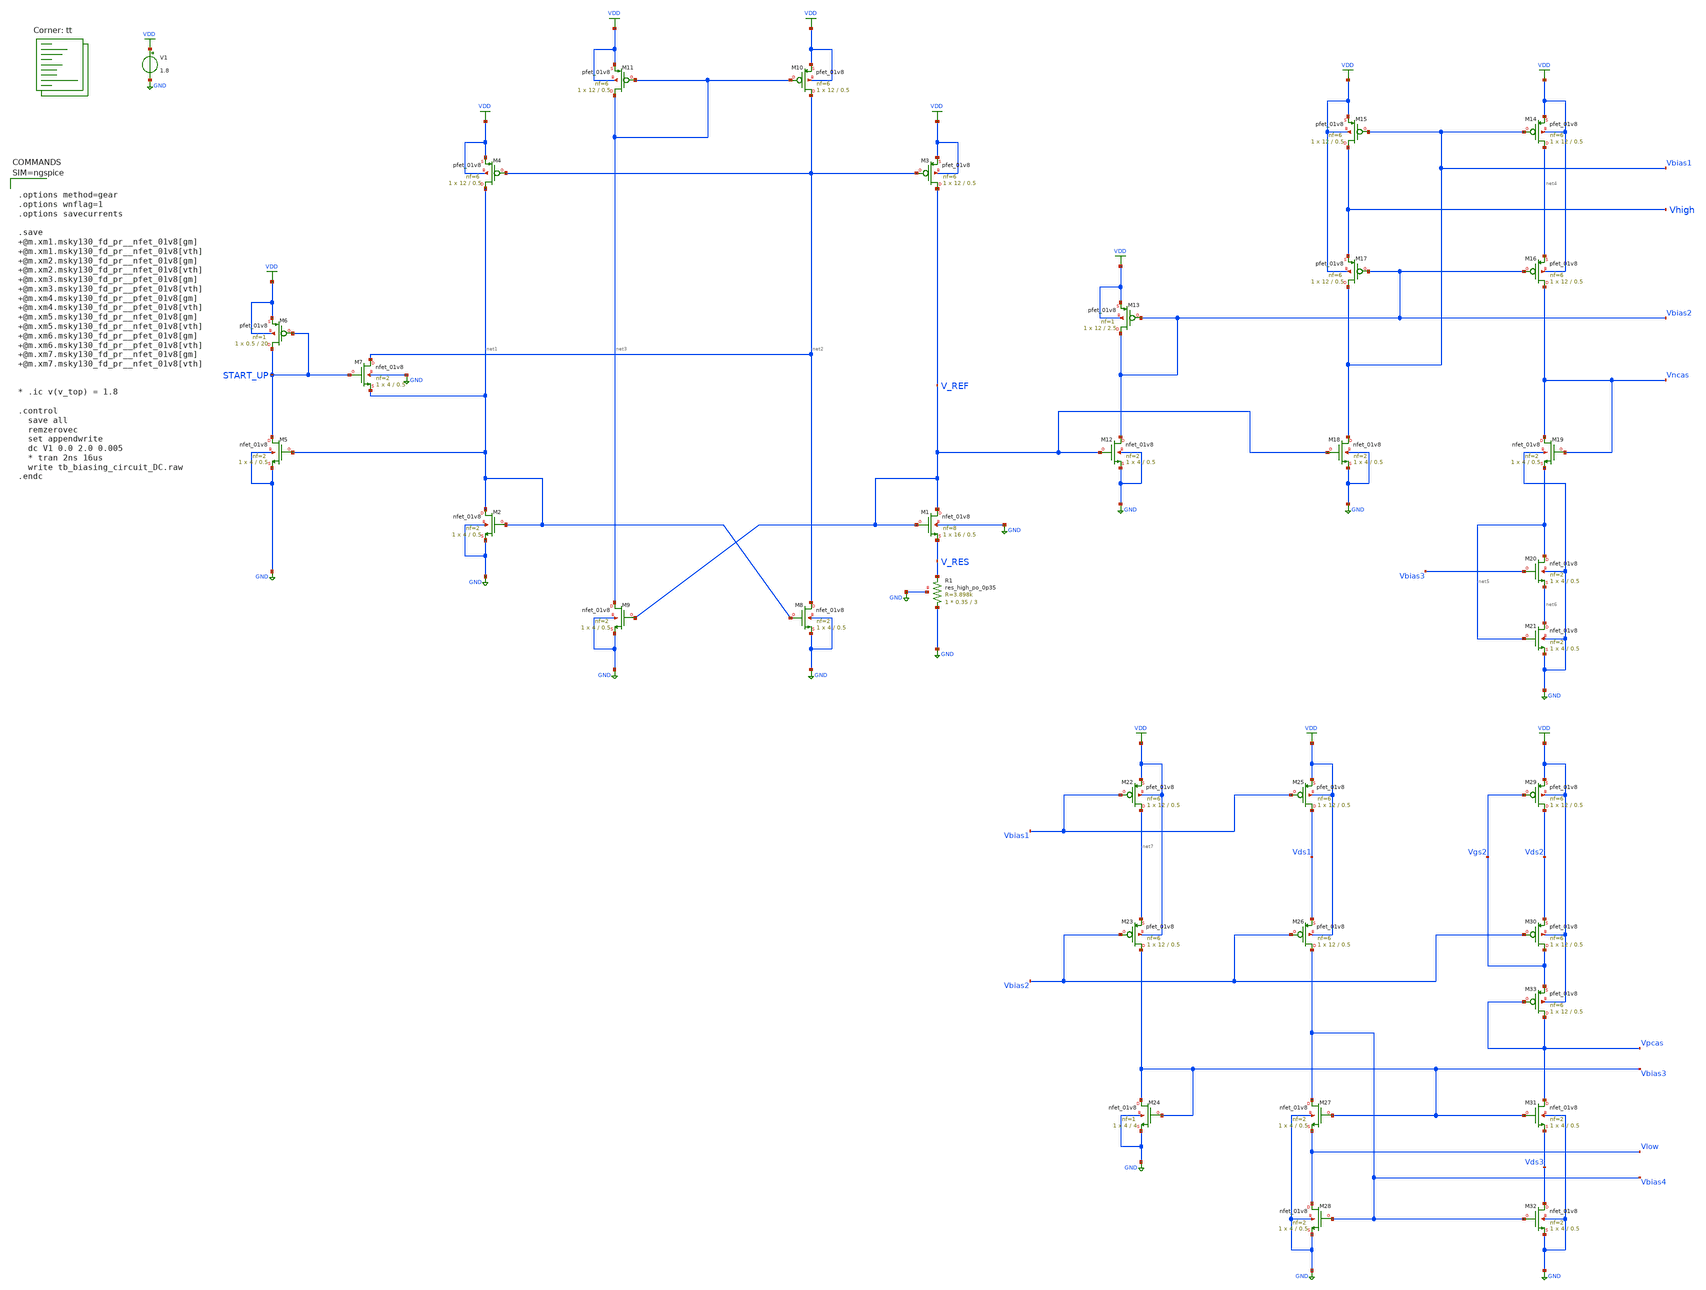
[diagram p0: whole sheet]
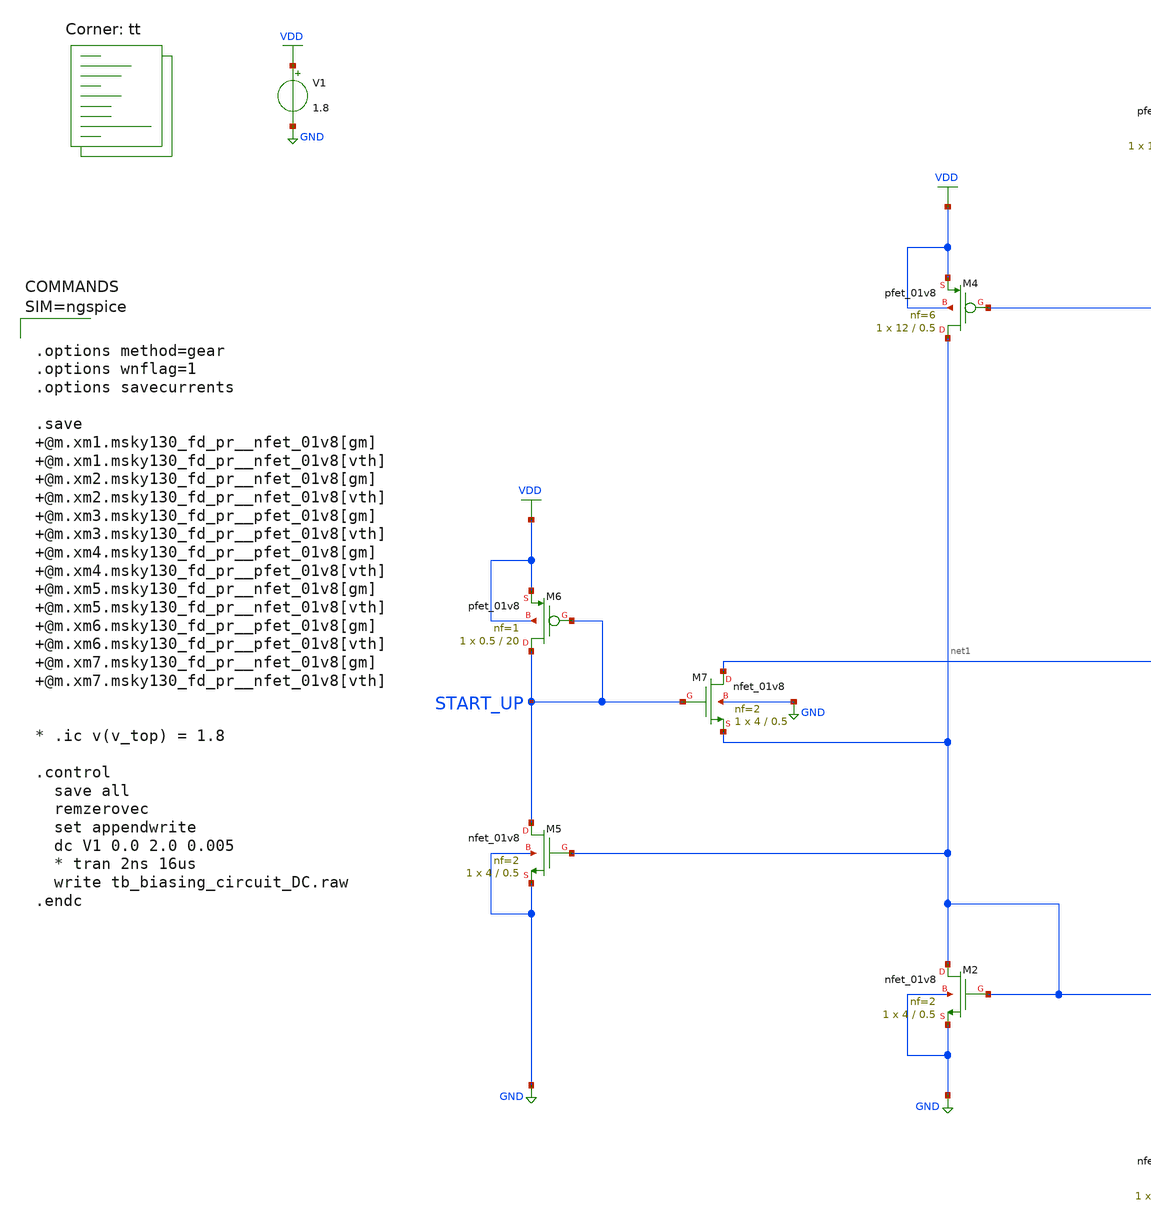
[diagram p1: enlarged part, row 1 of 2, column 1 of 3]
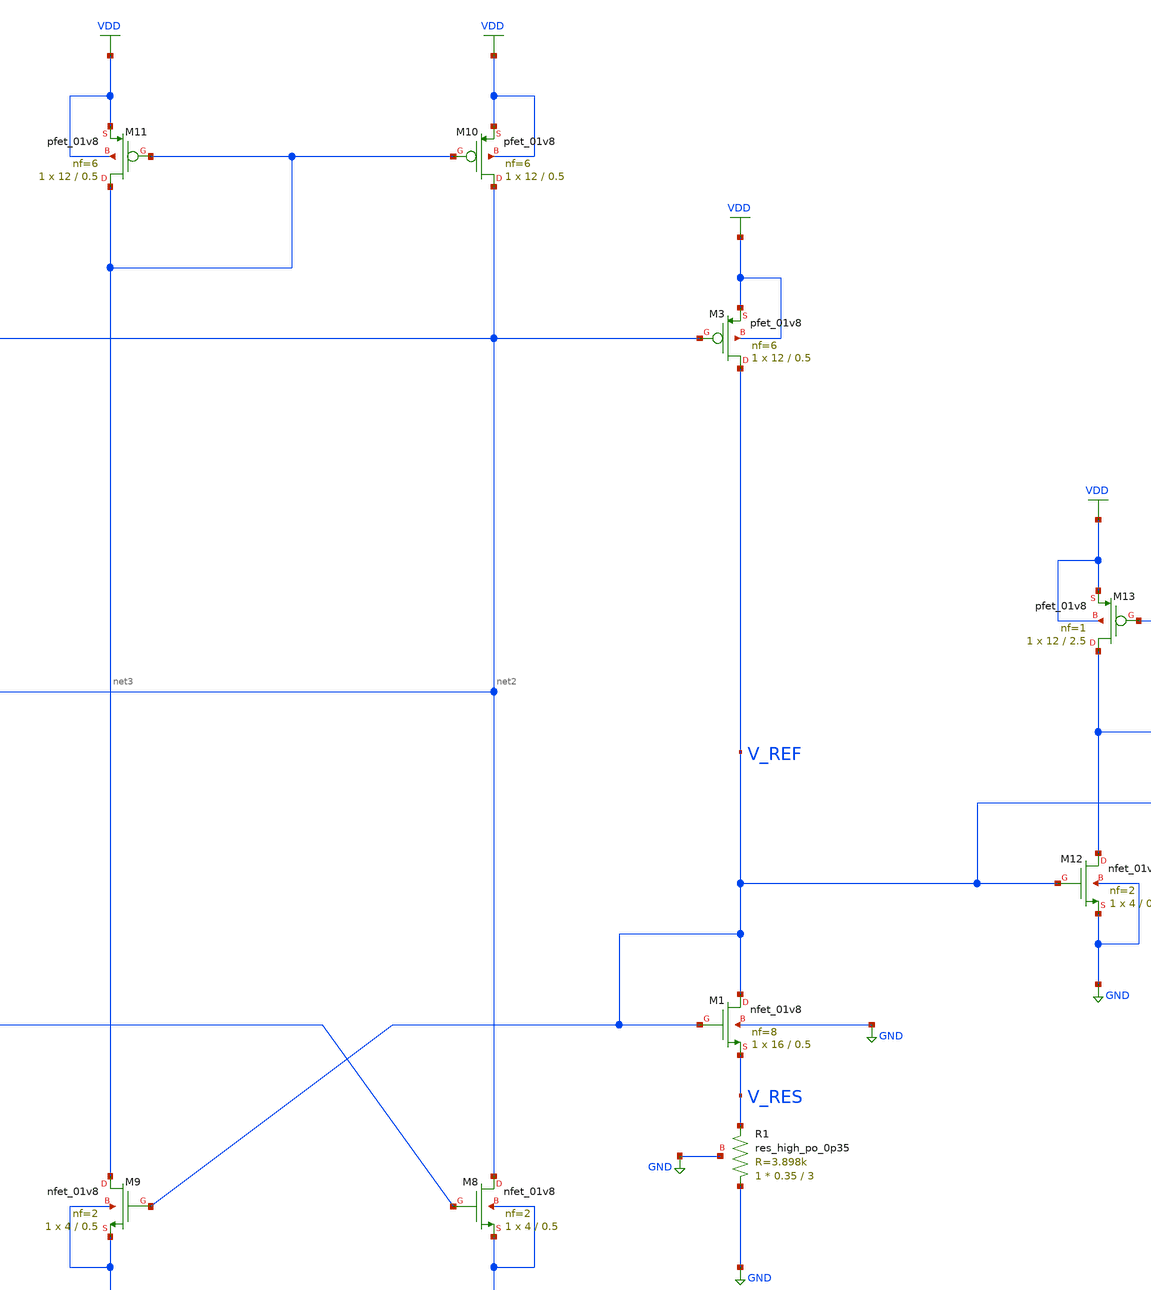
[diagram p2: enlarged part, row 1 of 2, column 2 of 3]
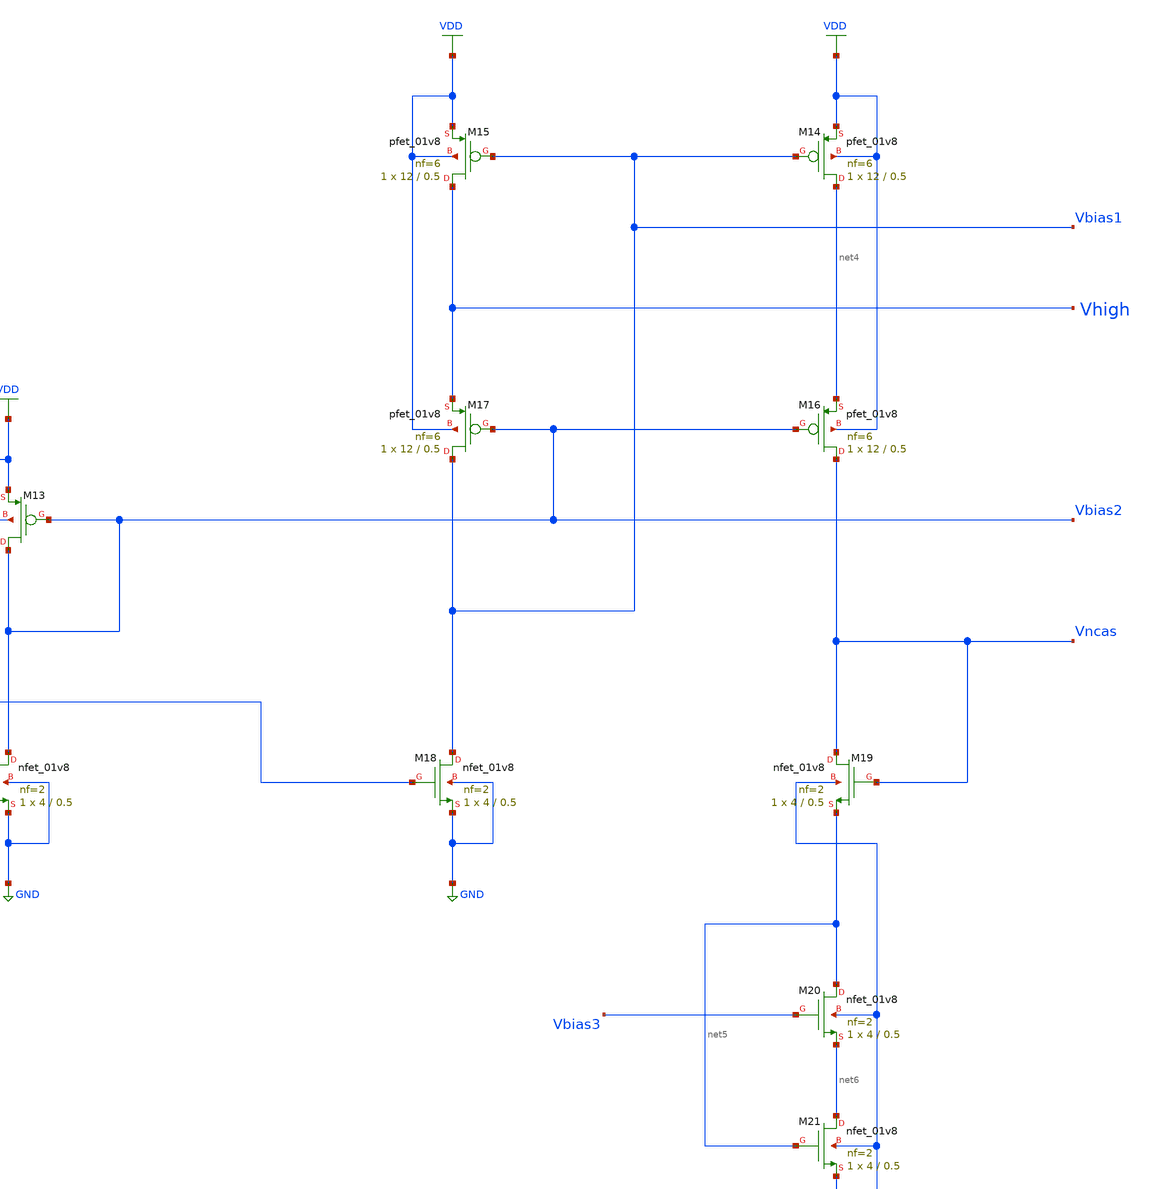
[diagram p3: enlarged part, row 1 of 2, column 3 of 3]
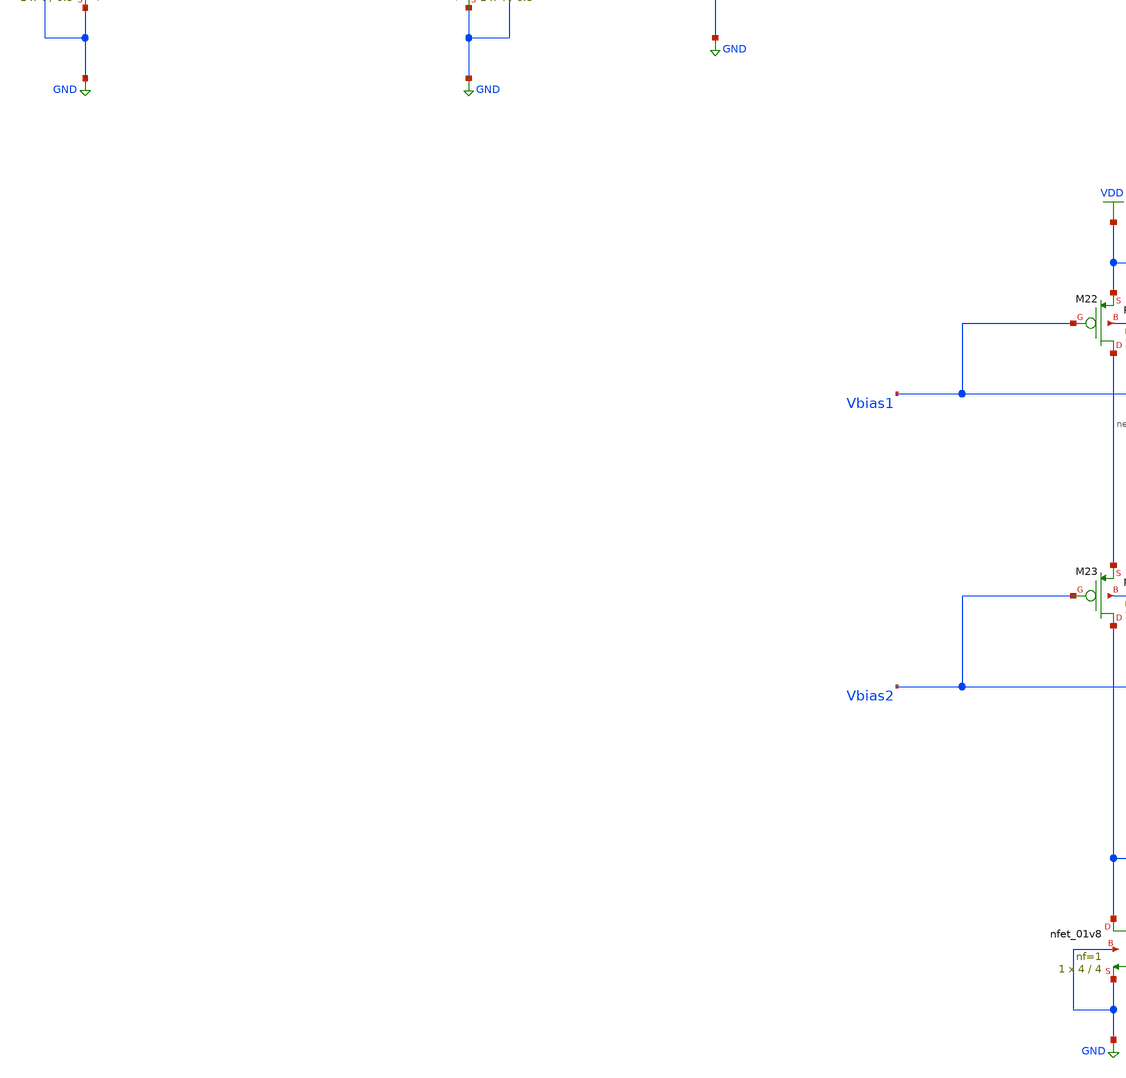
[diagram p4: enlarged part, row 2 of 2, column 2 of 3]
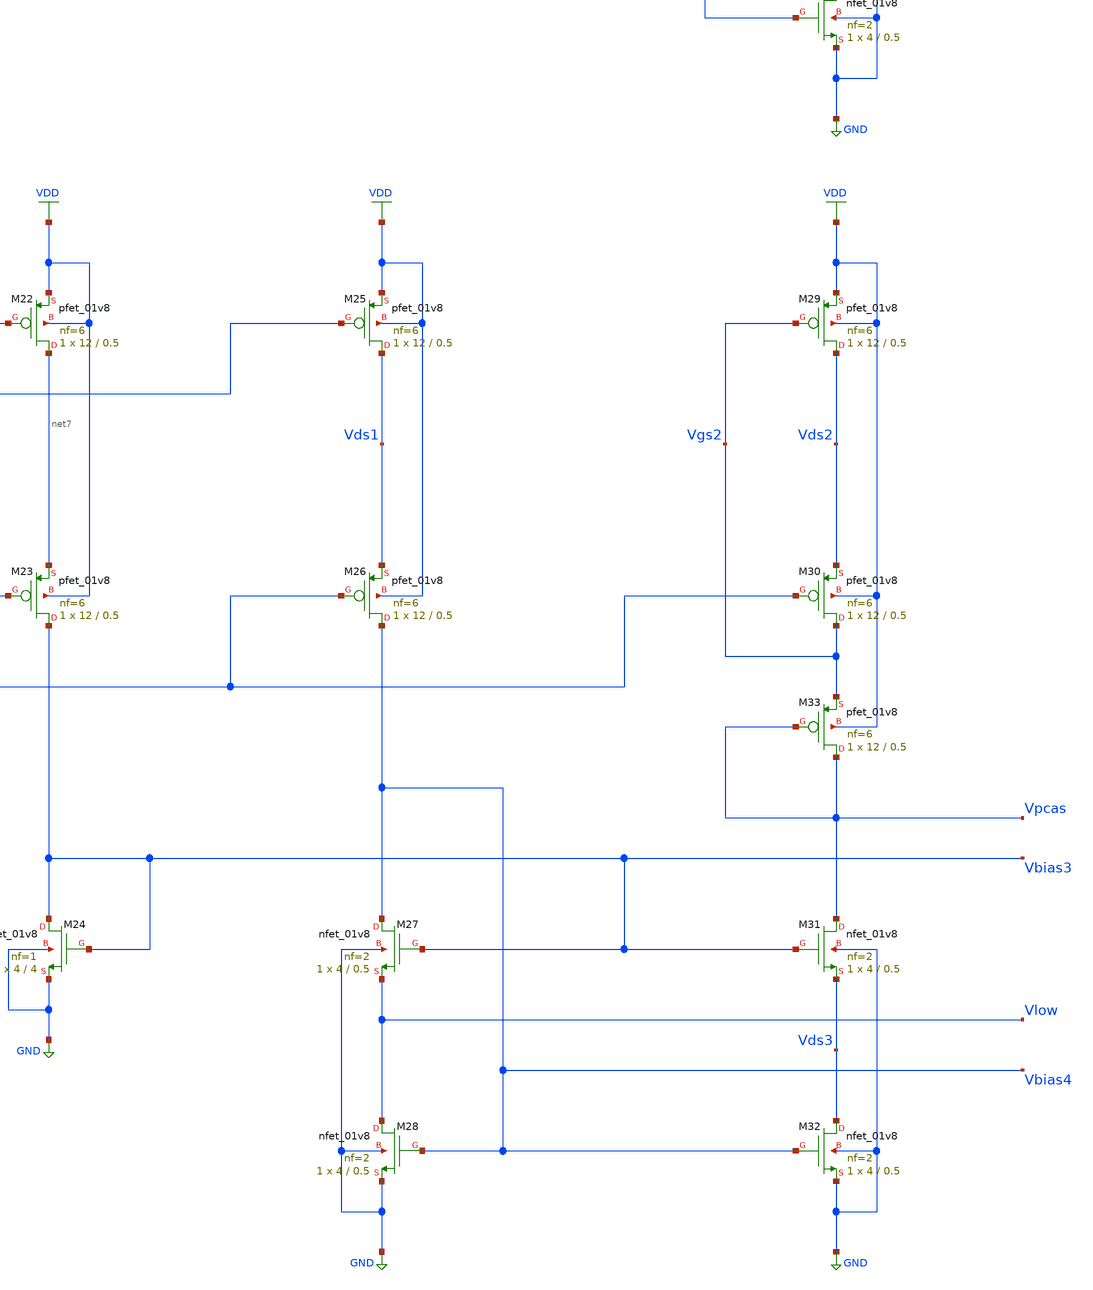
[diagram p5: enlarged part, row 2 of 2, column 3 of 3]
** sch_path: projects/ASU/EEE572/schematic/tb_biasing_circuit_DC.sch
**.subckt tb_biasing_circuit_DC
V1 VDD GND 1.8
XM1 V_REF V_REF V_RES GND sky130_fd_pr__nfet_01v8 L=0.5 W=16 nf=8 ad='int((nf+1)/2) * W/nf * 0.29' as='int((nf+2)/2) * W/nf * 0.29'
+ pd='2*int((nf+1)/2) * (W/nf + 0.29)' ps='2*int((nf+2)/2) * (W/nf + 0.29)' nrd='0.29 / W' nrs='0.29 / W'
+ sa=0 sb=0 sd=0 mult=1 m=1
XM2 net1 net1 GND GND sky130_fd_pr__nfet_01v8 L=0.5 W=4 nf=2 ad='int((nf+1)/2) * W/nf * 0.29' as='int((nf+2)/2) * W/nf * 0.29'
+ pd='2*int((nf+1)/2) * (W/nf + 0.29)' ps='2*int((nf+2)/2) * (W/nf + 0.29)' nrd='0.29 / W' nrs='0.29 / W'
+ sa=0 sb=0 sd=0 mult=1 m=1
XM5 START_UP net1 GND GND sky130_fd_pr__nfet_01v8 L=0.5 W=4 nf=2 ad='int((nf+1)/2) * W/nf * 0.29' as='int((nf+2)/2) * W/nf * 0.29'
+ pd='2*int((nf+1)/2) * (W/nf + 0.29)' ps='2*int((nf+2)/2) * (W/nf + 0.29)' nrd='0.29 / W' nrs='0.29 / W'
+ sa=0 sb=0 sd=0 mult=1 m=1
XM7 net2 START_UP net1 GND sky130_fd_pr__nfet_01v8 L=0.5 W=4 nf=2 ad='int((nf+1)/2) * W/nf * 0.29' as='int((nf+2)/2) * W/nf * 0.29'
+ pd='2*int((nf+1)/2) * (W/nf + 0.29)' ps='2*int((nf+2)/2) * (W/nf + 0.29)' nrd='0.29 / W' nrs='0.29 / W'
+ sa=0 sb=0 sd=0 mult=1 m=1
XR1 GND V_RES GND sky130_fd_pr__res_high_po_0p35 L=3 mult=1 m=1
XM6 START_UP START_UP VDD VDD sky130_fd_pr__pfet_01v8 L=20 W=0.5 nf=1 ad='int((nf+1)/2) * W/nf * 0.29'
+ as='int((nf+2)/2) * W/nf * 0.29' pd='2*int((nf+1)/2) * (W/nf + 0.29)' ps='2*int((nf+2)/2) * (W/nf + 0.29)'
+ nrd='0.29 / W' nrs='0.29 / W' sa=0 sb=0 sd=0 mult=1 m=1
XM3 V_REF net2 VDD VDD sky130_fd_pr__pfet_01v8 L=0.5 W=12 nf=6 ad='int((nf+1)/2) * W/nf * 0.29' as='int((nf+2)/2) * W/nf * 0.29'
+ pd='2*int((nf+1)/2) * (W/nf + 0.29)' ps='2*int((nf+2)/2) * (W/nf + 0.29)' nrd='0.29 / W' nrs='0.29 / W'
+ sa=0 sb=0 sd=0 mult=1 m=1
XM4 net1 net2 VDD VDD sky130_fd_pr__pfet_01v8 L=0.5 W=12 nf=6 ad='int((nf+1)/2) * W/nf * 0.29' as='int((nf+2)/2) * W/nf * 0.29'
+ pd='2*int((nf+1)/2) * (W/nf + 0.29)' ps='2*int((nf+2)/2) * (W/nf + 0.29)' nrd='0.29 / W' nrs='0.29 / W'
+ sa=0 sb=0 sd=0 mult=1 m=1
XM8 net2 net1 GND GND sky130_fd_pr__nfet_01v8 L=0.5 W=4 nf=2 ad='int((nf+1)/2) * W/nf * 0.29' as='int((nf+2)/2) * W/nf * 0.29'
+ pd='2*int((nf+1)/2) * (W/nf + 0.29)' ps='2*int((nf+2)/2) * (W/nf + 0.29)' nrd='0.29 / W' nrs='0.29 / W'
+ sa=0 sb=0 sd=0 mult=1 m=1
XM9 net3 V_REF GND GND sky130_fd_pr__nfet_01v8 L=0.5 W=4 nf=2 ad='int((nf+1)/2) * W/nf * 0.29' as='int((nf+2)/2) * W/nf * 0.29'
+ pd='2*int((nf+1)/2) * (W/nf + 0.29)' ps='2*int((nf+2)/2) * (W/nf + 0.29)' nrd='0.29 / W' nrs='0.29 / W'
+ sa=0 sb=0 sd=0 mult=1 m=1
XM10 net2 net3 VDD VDD sky130_fd_pr__pfet_01v8 L=0.5 W=12 nf=6 ad='int((nf+1)/2) * W/nf * 0.29' as='int((nf+2)/2) * W/nf * 0.29'
+ pd='2*int((nf+1)/2) * (W/nf + 0.29)' ps='2*int((nf+2)/2) * (W/nf + 0.29)' nrd='0.29 / W' nrs='0.29 / W'
+ sa=0 sb=0 sd=0 mult=1 m=1
XM11 net3 net3 VDD VDD sky130_fd_pr__pfet_01v8 L=0.5 W=12 nf=6 ad='int((nf+1)/2) * W/nf * 0.29' as='int((nf+2)/2) * W/nf * 0.29'
+ pd='2*int((nf+1)/2) * (W/nf + 0.29)' ps='2*int((nf+2)/2) * (W/nf + 0.29)' nrd='0.29 / W' nrs='0.29 / W'
+ sa=0 sb=0 sd=0 mult=1 m=1
XM12 Vbias2 V_REF GND GND sky130_fd_pr__nfet_01v8 L=0.5 W=4 nf=2 ad='int((nf+1)/2) * W/nf * 0.29' as='int((nf+2)/2) * W/nf * 0.29'
+ pd='2*int((nf+1)/2) * (W/nf + 0.29)' ps='2*int((nf+2)/2) * (W/nf + 0.29)' nrd='0.29 / W' nrs='0.29 / W'
+ sa=0 sb=0 sd=0 mult=1 m=1
XM13 Vbias2 Vbias2 VDD VDD sky130_fd_pr__pfet_01v8 L=2.5 W=12 nf=1 ad='int((nf+1)/2) * W/nf * 0.29' as='int((nf+2)/2) * W/nf * 0.29'
+ pd='2*int((nf+1)/2) * (W/nf + 0.29)' ps='2*int((nf+2)/2) * (W/nf + 0.29)' nrd='0.29 / W' nrs='0.29 / W'
+ sa=0 sb=0 sd=0 mult=1 m=1
XM14 net4 Vbias1 VDD VDD sky130_fd_pr__pfet_01v8 L=0.5 W=12 nf=6 ad='int((nf+1)/2) * W/nf * 0.29' as='int((nf+2)/2) * W/nf * 0.29'
+ pd='2*int((nf+1)/2) * (W/nf + 0.29)' ps='2*int((nf+2)/2) * (W/nf + 0.29)' nrd='0.29 / W' nrs='0.29 / W'
+ sa=0 sb=0 sd=0 mult=1 m=1
XM15 Vhigh Vbias1 VDD VDD sky130_fd_pr__pfet_01v8 L=0.5 W=12 nf=6 ad='int((nf+1)/2) * W/nf * 0.29' as='int((nf+2)/2) * W/nf * 0.29'
+ pd='2*int((nf+1)/2) * (W/nf + 0.29)' ps='2*int((nf+2)/2) * (W/nf + 0.29)' nrd='0.29 / W' nrs='0.29 / W'
+ sa=0 sb=0 sd=0 mult=1 m=1
XM16 Vncas Vbias2 net4 VDD sky130_fd_pr__pfet_01v8 L=0.5 W=12 nf=6 ad='int((nf+1)/2) * W/nf * 0.29' as='int((nf+2)/2) * W/nf * 0.29'
+ pd='2*int((nf+1)/2) * (W/nf + 0.29)' ps='2*int((nf+2)/2) * (W/nf + 0.29)' nrd='0.29 / W' nrs='0.29 / W'
+ sa=0 sb=0 sd=0 mult=1 m=1
XM17 Vbias1 Vbias2 Vhigh VDD sky130_fd_pr__pfet_01v8 L=0.5 W=12 nf=6 ad='int((nf+1)/2) * W/nf * 0.29'
+ as='int((nf+2)/2) * W/nf * 0.29' pd='2*int((nf+1)/2) * (W/nf + 0.29)' ps='2*int((nf+2)/2) * (W/nf + 0.29)'
+ nrd='0.29 / W' nrs='0.29 / W' sa=0 sb=0 sd=0 mult=1 m=1
XM18 Vbias1 V_REF GND GND sky130_fd_pr__nfet_01v8 L=0.5 W=4 nf=2 ad='int((nf+1)/2) * W/nf * 0.29' as='int((nf+2)/2) * W/nf * 0.29'
+ pd='2*int((nf+1)/2) * (W/nf + 0.29)' ps='2*int((nf+2)/2) * (W/nf + 0.29)' nrd='0.29 / W' nrs='0.29 / W'
+ sa=0 sb=0 sd=0 mult=1 m=1
XM19 Vncas Vncas net5 GND sky130_fd_pr__nfet_01v8 L=0.5 W=4 nf=2 ad='int((nf+1)/2) * W/nf * 0.29' as='int((nf+2)/2) * W/nf * 0.29'
+ pd='2*int((nf+1)/2) * (W/nf + 0.29)' ps='2*int((nf+2)/2) * (W/nf + 0.29)' nrd='0.29 / W' nrs='0.29 / W'
+ sa=0 sb=0 sd=0 mult=1 m=1
XM20 net5 Vbias3 net6 GND sky130_fd_pr__nfet_01v8 L=0.5 W=4 nf=2 ad='int((nf+1)/2) * W/nf * 0.29' as='int((nf+2)/2) * W/nf * 0.29'
+ pd='2*int((nf+1)/2) * (W/nf + 0.29)' ps='2*int((nf+2)/2) * (W/nf + 0.29)' nrd='0.29 / W' nrs='0.29 / W'
+ sa=0 sb=0 sd=0 mult=1 m=1
XM21 net6 net5 GND GND sky130_fd_pr__nfet_01v8 L=0.5 W=4 nf=2 ad='int((nf+1)/2) * W/nf * 0.29' as='int((nf+2)/2) * W/nf * 0.29'
+ pd='2*int((nf+1)/2) * (W/nf + 0.29)' ps='2*int((nf+2)/2) * (W/nf + 0.29)' nrd='0.29 / W' nrs='0.29 / W'
+ sa=0 sb=0 sd=0 mult=1 m=1
XM22 net7 Vbias1 VDD VDD sky130_fd_pr__pfet_01v8 L=0.5 W=12 nf=6 ad='int((nf+1)/2) * W/nf * 0.29' as='int((nf+2)/2) * W/nf * 0.29'
+ pd='2*int((nf+1)/2) * (W/nf + 0.29)' ps='2*int((nf+2)/2) * (W/nf + 0.29)' nrd='0.29 / W' nrs='0.29 / W'
+ sa=0 sb=0 sd=0 mult=1 m=1
XM23 Vbias3 Vbias2 net7 VDD sky130_fd_pr__pfet_01v8 L=0.5 W=12 nf=6 ad='int((nf+1)/2) * W/nf * 0.29'
+ as='int((nf+2)/2) * W/nf * 0.29' pd='2*int((nf+1)/2) * (W/nf + 0.29)' ps='2*int((nf+2)/2) * (W/nf + 0.29)'
+ nrd='0.29 / W' nrs='0.29 / W' sa=0 sb=0 sd=0 mult=1 m=1
XM24 Vbias3 Vbias3 GND GND sky130_fd_pr__nfet_01v8 L=4 W=4 nf=1 ad='int((nf+1)/2) * W/nf * 0.29' as='int((nf+2)/2) * W/nf * 0.29'
+ pd='2*int((nf+1)/2) * (W/nf + 0.29)' ps='2*int((nf+2)/2) * (W/nf + 0.29)' nrd='0.29 / W' nrs='0.29 / W'
+ sa=0 sb=0 sd=0 mult=1 m=1
XM25 Vds1 Vbias1 VDD VDD sky130_fd_pr__pfet_01v8 L=0.5 W=12 nf=6 ad='int((nf+1)/2) * W/nf * 0.29' as='int((nf+2)/2) * W/nf * 0.29'
+ pd='2*int((nf+1)/2) * (W/nf + 0.29)' ps='2*int((nf+2)/2) * (W/nf + 0.29)' nrd='0.29 / W' nrs='0.29 / W'
+ sa=0 sb=0 sd=0 mult=1 m=1
XM26 Vbias4 Vbias2 Vds1 VDD sky130_fd_pr__pfet_01v8 L=0.5 W=12 nf=6 ad='int((nf+1)/2) * W/nf * 0.29'
+ as='int((nf+2)/2) * W/nf * 0.29' pd='2*int((nf+1)/2) * (W/nf + 0.29)' ps='2*int((nf+2)/2) * (W/nf + 0.29)'
+ nrd='0.29 / W' nrs='0.29 / W' sa=0 sb=0 sd=0 mult=1 m=1
XM27 Vbias4 Vbias3 Vlow GND sky130_fd_pr__nfet_01v8 L=0.5 W=4 nf=2 ad='int((nf+1)/2) * W/nf * 0.29' as='int((nf+2)/2) * W/nf * 0.29'
+ pd='2*int((nf+1)/2) * (W/nf + 0.29)' ps='2*int((nf+2)/2) * (W/nf + 0.29)' nrd='0.29 / W' nrs='0.29 / W'
+ sa=0 sb=0 sd=0 mult=1 m=1
XM28 Vlow Vbias4 GND GND sky130_fd_pr__nfet_01v8 L=0.5 W=4 nf=2 ad='int((nf+1)/2) * W/nf * 0.29' as='int((nf+2)/2) * W/nf * 0.29'
+ pd='2*int((nf+1)/2) * (W/nf + 0.29)' ps='2*int((nf+2)/2) * (W/nf + 0.29)' nrd='0.29 / W' nrs='0.29 / W'
+ sa=0 sb=0 sd=0 mult=1 m=1
XM29 Vds2 Vgs2 VDD VDD sky130_fd_pr__pfet_01v8 L=0.5 W=12 nf=6 ad='int((nf+1)/2) * W/nf * 0.29' as='int((nf+2)/2) * W/nf * 0.29'
+ pd='2*int((nf+1)/2) * (W/nf + 0.29)' ps='2*int((nf+2)/2) * (W/nf + 0.29)' nrd='0.29 / W' nrs='0.29 / W'
+ sa=0 sb=0 sd=0 mult=1 m=1
XM30 Vgs2 Vbias2 Vds2 VDD sky130_fd_pr__pfet_01v8 L=0.5 W=12 nf=6 ad='int((nf+1)/2) * W/nf * 0.29' as='int((nf+2)/2) * W/nf * 0.29'
+ pd='2*int((nf+1)/2) * (W/nf + 0.29)' ps='2*int((nf+2)/2) * (W/nf + 0.29)' nrd='0.29 / W' nrs='0.29 / W'
+ sa=0 sb=0 sd=0 mult=1 m=1
XM31 Vpcas Vbias3 Vds3 GND sky130_fd_pr__nfet_01v8 L=0.5 W=4 nf=2 ad='int((nf+1)/2) * W/nf * 0.29' as='int((nf+2)/2) * W/nf * 0.29'
+ pd='2*int((nf+1)/2) * (W/nf + 0.29)' ps='2*int((nf+2)/2) * (W/nf + 0.29)' nrd='0.29 / W' nrs='0.29 / W'
+ sa=0 sb=0 sd=0 mult=1 m=1
XM32 Vds3 Vbias4 GND GND sky130_fd_pr__nfet_01v8 L=0.5 W=4 nf=2 ad='int((nf+1)/2) * W/nf * 0.29' as='int((nf+2)/2) * W/nf * 0.29'
+ pd='2*int((nf+1)/2) * (W/nf + 0.29)' ps='2*int((nf+2)/2) * (W/nf + 0.29)' nrd='0.29 / W' nrs='0.29 / W'
+ sa=0 sb=0 sd=0 mult=1 m=1
XM33 Vpcas Vpcas Vgs2 VDD sky130_fd_pr__pfet_01v8 L=0.5 W=12 nf=6 ad='int((nf+1)/2) * W/nf * 0.29' as='int((nf+2)/2) * W/nf * 0.29'
+ pd='2*int((nf+1)/2) * (W/nf + 0.29)' ps='2*int((nf+2)/2) * (W/nf + 0.29)' nrd='0.29 / W' nrs='0.29 / W'
+ sa=0 sb=0 sd=0 mult=1 m=1
**** begin user architecture code
.lib $::SKYWATER_MODELS/sky130.lib.spice tt



.options method=gear
.options wnflag=1
.options savecurrents

.save @m.xm1.msky130_fd_pr__nfet_01v8[gm] @m.xm1.msky130_fd_pr__nfet_01v8[vth] @m.xm2.msky130_fd_pr__nfet_01v8[gm] @m.xm2.msky130_fd_pr__nfet_01v8[vth] @m.xm3.msky130_fd_pr__pfet_01v8[gm] @m.xm3.msky130_fd_pr__pfet_01v8[vth] @m.xm4.msky130_fd_pr__pfet_01v8[gm] @m.xm4.msky130_fd_pr__pfet_01v8[vth] @m.xm5.msky130_fd_pr__nfet_01v8[gm] @m.xm5.msky130_fd_pr__nfet_01v8[vth] @m.xm6.msky130_fd_pr__pfet_01v8[gm] @m.xm6.msky130_fd_pr__pfet_01v8[vth] @m.xm7.msky130_fd_pr__nfet_01v8[gm] @m.xm7.msky130_fd_pr__nfet_01v8[vth]


* .ic v(v_top) = 1.8

.control
  save all
  remzerovec
  set appendwrite
  dc V1 0.0 2.0 0.005
  * tran 2ns 16us
  write tb_biasing_circuit_DC.raw
.endc





**** end user architecture code
**.ends
.GLOBAL GND
.GLOBAL VDD
.end
